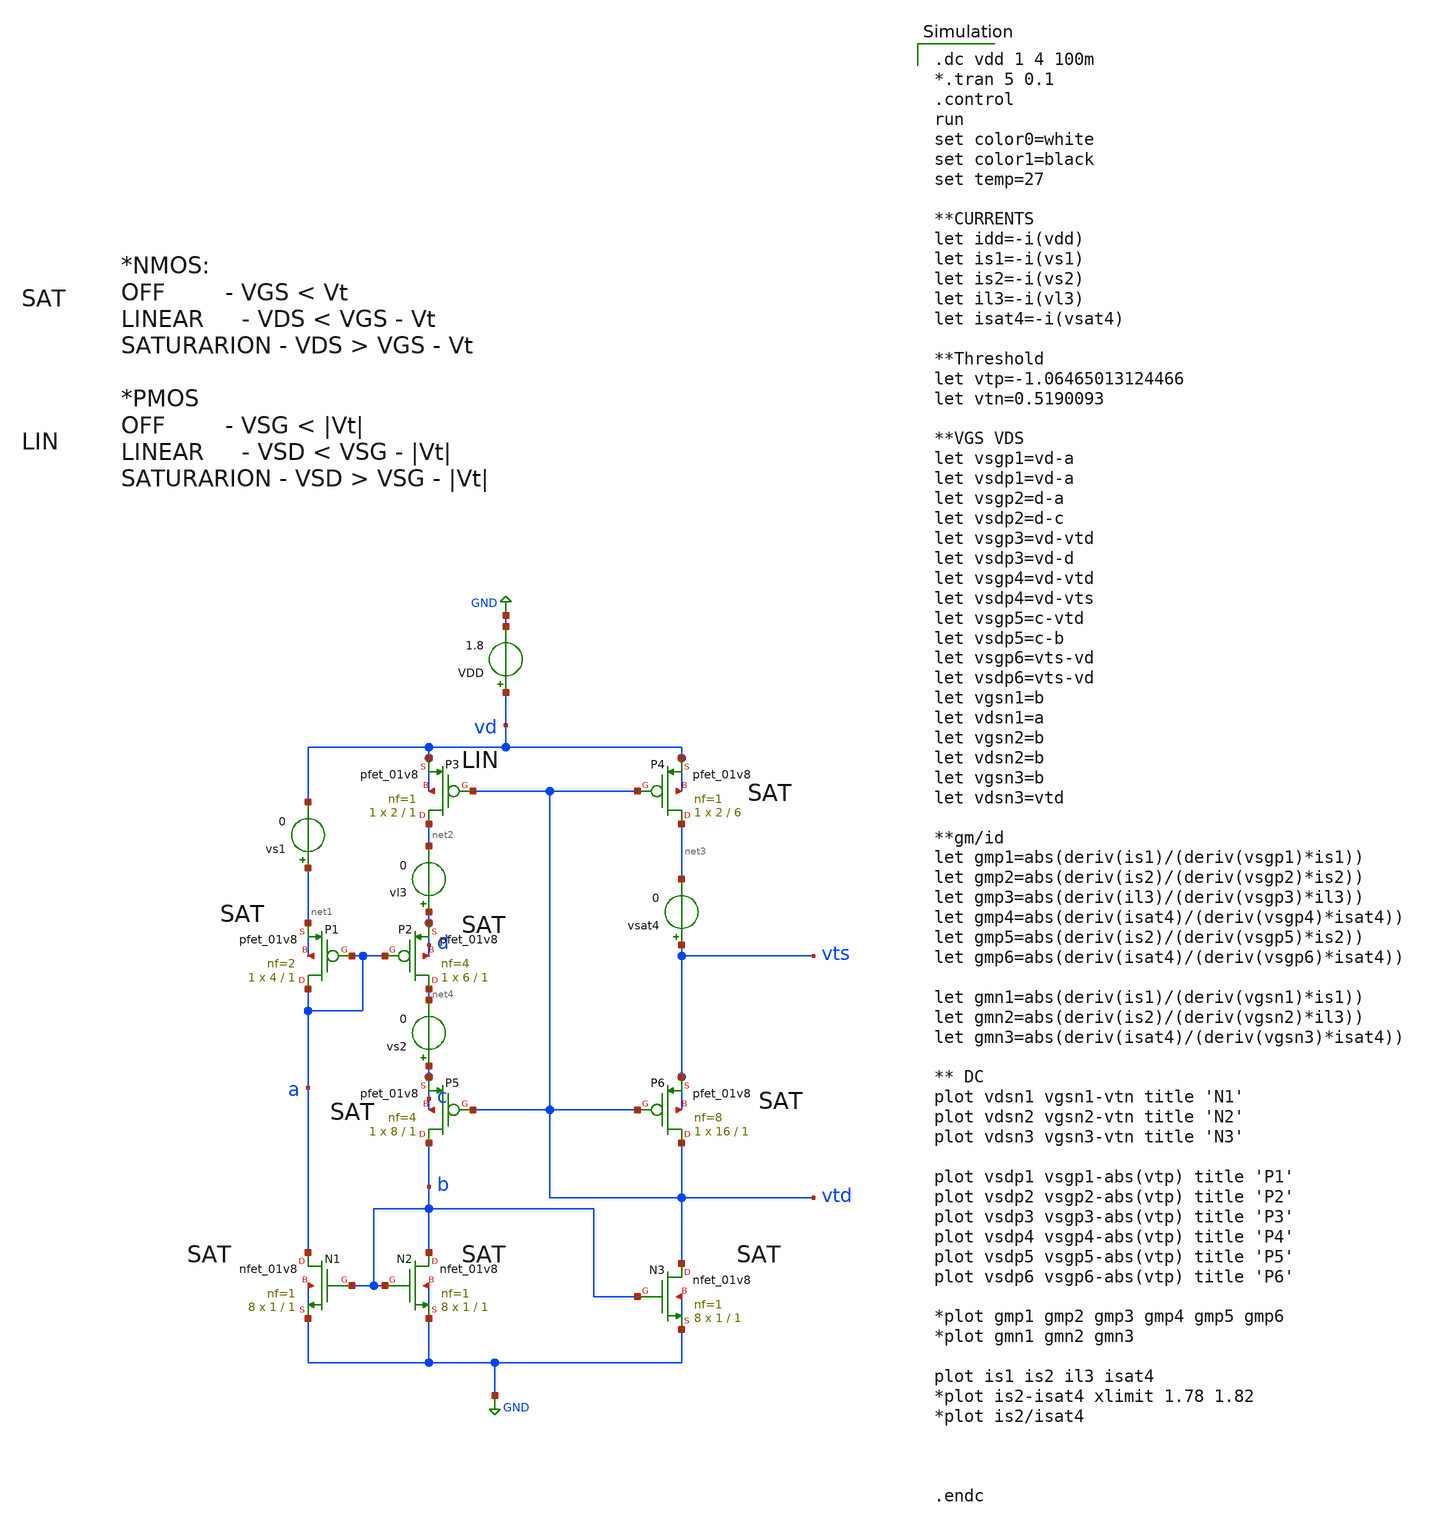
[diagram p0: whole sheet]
** sch_path: sensor/xschem/temp-tb-dc.sch
**.subckt temp-tb-dc
VDD vd GND 1.8
vs1 net1 vd 0
vs2 c net4 0
vl3 d net2 0
vsat4 vts net3 0
XP1 a a net1 net1 sky130_fd_pr__pfet_01v8 L=1 W=4 nf=2 ad='int((nf+1)/2) * W/nf * 0.29' as='int((nf+2)/2) * W/nf * 0.29'
+ pd='2*int((nf+1)/2) * (W/nf + 0.29)' ps='2*int((nf+2)/2) * (W/nf + 0.29)' nrd='0.29 / W' nrs='0.29 / W'
+ sa=0 sb=0 sd=0 mult=1 m=1
XP2 net4 a d d sky130_fd_pr__pfet_01v8 L=1 W=6 nf=4 ad='int((nf+1)/2) * W/nf * 0.29' as='int((nf+2)/2) * W/nf * 0.29'
+ pd='2*int((nf+1)/2) * (W/nf + 0.29)' ps='2*int((nf+2)/2) * (W/nf + 0.29)' nrd='0.29 / W' nrs='0.29 / W'
+ sa=0 sb=0 sd=0 mult=1 m=1
XP3 net2 vtd vd vd sky130_fd_pr__pfet_01v8 L=1 W=2 nf=1 ad='int((nf+1)/2) * W/nf * 0.29' as='int((nf+2)/2) * W/nf * 0.29'
+ pd='2*int((nf+1)/2) * (W/nf + 0.29)' ps='2*int((nf+2)/2) * (W/nf + 0.29)' nrd='0.29 / W' nrs='0.29 / W'
+ sa=0 sb=0 sd=0 mult=1 m=1
XP4 net3 vtd vd vd sky130_fd_pr__pfet_01v8 L=6 W=2 nf=1 ad='int((nf+1)/2) * W/nf * 0.29' as='int((nf+2)/2) * W/nf * 0.29'
+ pd='2*int((nf+1)/2) * (W/nf + 0.29)' ps='2*int((nf+2)/2) * (W/nf + 0.29)' nrd='0.29 / W' nrs='0.29 / W'
+ sa=0 sb=0 sd=0 mult=1 m=1
XP5 b vtd c c sky130_fd_pr__pfet_01v8 L=1 W=8 nf=4 ad='int((nf+1)/2) * W/nf * 0.29' as='int((nf+2)/2) * W/nf * 0.29'
+ pd='2*int((nf+1)/2) * (W/nf + 0.29)' ps='2*int((nf+2)/2) * (W/nf + 0.29)' nrd='0.29 / W' nrs='0.29 / W'
+ sa=0 sb=0 sd=0 mult=1 m=1
XP6 vtd vtd vts vts sky130_fd_pr__pfet_01v8 L=1 W=16 nf=8 ad='int((nf+1)/2) * W/nf * 0.29' as='int((nf+2)/2) * W/nf * 0.29'
+ pd='2*int((nf+1)/2) * (W/nf + 0.29)' ps='2*int((nf+2)/2) * (W/nf + 0.29)' nrd='0.29 / W' nrs='0.29 / W'
+ sa=0 sb=0 sd=0 mult=1 m=1
XN1 a b GND GND sky130_fd_pr__nfet_01v8 L=1 W=1 nf=1 ad='int((nf+1)/2) * W/nf * 0.29' as='int((nf+2)/2) * W/nf * 0.29'
+ pd='2*int((nf+1)/2) * (W/nf + 0.29)' ps='2*int((nf+2)/2) * (W/nf + 0.29)' nrd='0.29 / W' nrs='0.29 / W'
+ sa=0 sb=0 sd=0 mult=8 m=8
XN2 b b GND GND sky130_fd_pr__nfet_01v8 L=1 W=1 nf=1 ad='int((nf+1)/2) * W/nf * 0.29' as='int((nf+2)/2) * W/nf * 0.29'
+ pd='2*int((nf+1)/2) * (W/nf + 0.29)' ps='2*int((nf+2)/2) * (W/nf + 0.29)' nrd='0.29 / W' nrs='0.29 / W'
+ sa=0 sb=0 sd=0 mult=8 m=8
XN3 vtd b GND GND sky130_fd_pr__nfet_01v8 L=1 W=1 nf=1 ad='int((nf+1)/2) * W/nf * 0.29' as='int((nf+2)/2) * W/nf * 0.29'
+ pd='2*int((nf+1)/2) * (W/nf + 0.29)' ps='2*int((nf+2)/2) * (W/nf + 0.29)' nrd='0.29 / W' nrs='0.29 / W'
+ sa=0 sb=0 sd=0 mult=8 m=8
**** begin user architecture code

.dc vdd 1 4 100m
*.tran 5 0.1
.control
run
set color0=white
set color1=black
set temp=27

**CURRENTS
let idd=-i(vdd)
let is1=-i(vs1)
let is2=-i(vs2)
let il3=-i(vl3)
let isat4=-i(vsat4)

**Threshold
let vtp=-1.06465013124466
let vtn=0.5190093

**VGS VDS
let vsgp1=vd-a
let vsdp1=vd-a
let vsgp2=d-a
let vsdp2=d-c
let vsgp3=vd-vtd
let vsdp3=vd-d
let vsgp4=vd-vtd
let vsdp4=vd-vts
let vsgp5=c-vtd
let vsdp5=c-b
let vsgp6=vts-vd
let vsdp6=vts-vd
let vgsn1=b
let vdsn1=a
let vgsn2=b
let vdsn2=b
let vgsn3=b
let vdsn3=vtd

**gm/id
let gmp1=abs(deriv(is1)/(deriv(vsgp1)*is1))
let gmp2=abs(deriv(is2)/(deriv(vsgp2)*is2))
let gmp3=abs(deriv(il3)/(deriv(vsgp3)*il3))
let gmp4=abs(deriv(isat4)/(deriv(vsgp4)*isat4))
let gmp5=abs(deriv(is2)/(deriv(vsgp5)*is2))
let gmp6=abs(deriv(isat4)/(deriv(vsgp6)*isat4))

let gmn1=abs(deriv(is1)/(deriv(vgsn1)*is1))
let gmn2=abs(deriv(is2)/(deriv(vgsn2)*il3))
let gmn3=abs(deriv(isat4)/(deriv(vgsn3)*isat4))

** DC
plot vdsn1 vgsn1-vtn title 'N1'
plot vdsn2 vgsn2-vtn title 'N2'
plot vdsn3 vgsn3-vtn title 'N3'

plot vsdp1 vsgp1-abs(vtp) title 'P1'
plot vsdp2 vsgp2-abs(vtp) title 'P2'
plot vsdp3 vsgp3-abs(vtp) title 'P3'
plot vsdp4 vsgp4-abs(vtp) title 'P4'
plot vsdp5 vsgp5-abs(vtp) title 'P5'
plot vsdp6 vsgp6-abs(vtp) title 'P6'

*plot gmp1 gmp2 gmp3 gmp4 gmp5 gmp6
*plot gmn1 gmn2 gmn3

plot is1 is2 il3 isat4
*plot is2-isat4 xlimit 1.78 1.82
*plot is2/isat4



.endc



.lib /home/hugodg/sky130_workspace/skywater-pdk/libraries/sky130_fd_pr_ngspice/latest/models/sky130.lib.spice tt



R0 a.n2 a.t0 63.907
R1 a.n3 a.t2 63.628
R2 a.n0 a.t5 63.628
R3 a.n0 a.t4 63.628
R4 a.n0 a.t6 63.628
R5 a.n1 a.t3 14.282
R6 a.n1 a.t1 14.282
R7 a.n0 a.n3 2.215
R8 a a.n0 1.033
R9 a.n2 a.n1 0.526
R10 a.n3 a.n2 0.258
R11 vd.n6 vd.n5 411.106
R12 vd.n7 vd.n6 271.662
R13 vd.n15 vd.n10 271.436
R14 vd.n16 vd.n15 143.96
R15 vd.n8 vd.n7 6.519
R16 vd.n18 vd.n8 4
R17 vd vd.n18 3.145
R18 vd.n17 vd.n16 0.327
R19 vd.n18 vd.n17 0.174
R20 vd.n15 vd.n14 0.015
R21 vd.n12 vd.n11 0.008
R22 vd.n10 vd.n9 0.008
R23 vd.n5 vd.n4 0.008
R24 vd.n13 vd.n12 0.007
R25 vd.n6 vd.n3 0.006
R26 vd.n14 vd.n13 0.003
R27 vd.n1 vd.n0 0.003
R28 vd.n2 vd.n1 0.003
R29 vd.n3 vd.n2 0.002
R30 vtd.n15 vtd.t19 64.071
R31 vtd.n4 vtd.t4 63.721
R32 vtd.n17 vtd.t20 63.628
R33 vtd.n16 vtd.t17 63.628
R34 vtd.n15 vtd.t18 63.628
R35 vtd.n14 vtd.t6 63.628
R36 vtd.n12 vtd.t10 63.628
R37 vtd.n11 vtd.t8 63.628
R38 vtd.n9 vtd.t12 63.628
R39 vtd.n8 vtd.t14 63.628
R40 vtd.n6 vtd.t0 63.628
R41 vtd.n5 vtd.t2 63.628
R42 vtd.n19 vtd.t16 14.917
R43 vtd.n3 vtd.t5 14.282
R44 vtd.n3 vtd.t3 14.282
R45 vtd.n2 vtd.t1 14.282
R46 vtd.n2 vtd.t15 14.282
R47 vtd.n1 vtd.t13 14.282
R48 vtd.n1 vtd.t9 14.282
R49 vtd.n0 vtd.t11 14.282
R50 vtd.n0 vtd.t7 14.282
R51 vtd.n18 vtd.n17 1.082
R52 vtd.n16 vtd.n15 0.443
R53 vtd.n17 vtd.n16 0.443
R54 vtd vtd.n19 0.162
R55 vtd.n18 vtd.n14 0.128
R56 vtd.n19 vtd.n18 0.118
R57 vtd.n14 vtd.n13 0.096
R58 vtd.n6 vtd.n5 0.089
R59 vtd.n9 vtd.n8 0.089
R60 vtd.n12 vtd.n11 0.089
R61 vtd.n4 vtd.n3 0.063
R62 vtd.n7 vtd.n2 0.063
R63 vtd.n10 vtd.n1 0.063
R64 vtd.n13 vtd.n0 0.063
R65 vtd.n5 vtd.n4 0.044
R66 vtd.n7 vtd.n6 0.044
R67 vtd.n8 vtd.n7 0.044
R68 vtd.n10 vtd.n9 0.044
R69 vtd.n11 vtd.n10 0.044
R70 vtd.n13 vtd.n12 0.044
R71 b.n20 b.t16 38.817
R72 b.n4 b.t19 38.791
R73 b.n7 b.t22 38.779
R74 b.n10 b.t18 38.769
R75 b.n13 b.t23 38.759
R76 b.n15 b.t17 38.749
R77 b.n18 b.t21 38.741
R78 b.n19 b.t20 38.731
R79 b.n21 b.t24 38.471
R80 b.n5 b.t27 38.458
R81 b.n8 b.t30 38.452
R82 b.n11 b.t26 38.447
R83 b.n23 b.t28 38.193
R84 b.n3 b.t25 38.104
R85 b.n2 b.t31 38.064
R86 b.n26 b.t29 38.058
R87 b.n15 b.t12 37.359
R88 b.n13 b.t0 37.359
R89 b.n4 b.t8 37.359
R90 b.n7 b.t2 37.359
R91 b.n10 b.t10 37.359
R92 b.n18 b.t4 37.359
R93 b.n19 b.t6 37.359
R94 b.n20 b.t14 37.359
R95 b.n5 b.t9 17.617
R96 b.n24 b.t7 17.404
R97 b.n17 b.t5 17.404
R98 b.n14 b.t13 17.404
R99 b.n12 b.t1 17.404
R100 b.n9 b.t11 17.404
R101 b.n6 b.t3 17.404
R102 b.n22 b.t15 17.404
R103 b b.n26 1.727
R104 b.n3 b.n2 0.75
R105 b.n26 b.n3 0.708
R106 b.n6 b.n5 0.392
R107 b.n9 b.n8 0.388
R108 b.n14 b.n1 0.379
R109 b.n17 b.n16 0.375
R110 b.n25 b.n24 0.371
R111 b.n23 b.n22 0.367
R112 b.n0 b.n11 0.352
R113 b.n21 b.n20 0.345
R114 b.n5 b.n4 0.332
R115 b.n8 b.n7 0.326
R116 b.n11 b.n10 0.321
R117 b.n16 b.n15 0.311
R118 b.n25 b.n18 0.307
R119 b.n26 b.n25 0.291
R120 b.n23 b.n19 0.286
R121 b.n1 b.n13 0.254
R122 b.n25 b.n17 0.233
R123 b.n16 b.n14 0.229
R124 b.n11 b.n9 0.221
R125 b.n8 b.n6 0.217
R126 b.n1 b.n12 0.212
R127 b.n22 b.n21 0.2
R128 b.n24 b.n23 0.196
R129 b.n1 b.n0 0.124
R130 gnd.n10 gnd.n12 732.611
R131 gnd.n10 gnd.n14 732.611
R132 gnd.n1 gnd.n3 732.611
R133 gnd.n1 gnd.n5 732.611
R134 gnd.n0 gnd.n7 732.611
R135 gnd.n0 gnd.n9 732.611
R136 gnd.n15 gnd.n1 3.25
R137 gnd.n16 gnd.n10 3.137
R138 gnd.n15 gnd.n0 2.717
R139 gnd gnd.n16 0.192
R140 gnd.n16 gnd.n15 0.101
R141 gnd.n12 gnd.n11 0.004
R142 gnd.n14 gnd.n13 0.004
R143 gnd.n3 gnd.n2 0.004
R144 gnd.n5 gnd.n4 0.004
R145 gnd.n7 gnd.n6 0.004
R146 gnd.n9 gnd.n8 0.004
C0 vts c 0.22fF
C1 a c 0.61fF
C2 c d 0.88fF
C3 vts vtd 3.97fF
C4 b vts 1.25fF
C5 a vtd 0.62fF
C6 vtd d 0.24fF
C7 b a 1.24fF
C8 b d 0.04fF
C9 vts vd 0.45fF
C10 c vtd 1.16fF
C11 a vd 1.17fF
C12 d vd 0.94fF
C13 b c 0.61fF
C14 c vd 0.43fF
C15 b vtd 4.68fF
C16 vtd vd 0.78fF
C17 b vd 0.11fF
C18 a vts 0.37fF
C19 vts d 0.05fF
C20 a d 0.78fF
C21 b.n0 gnd 0.04fF $ **FLOATING
C22 b.n1 gnd 0.15fF $ **FLOATING
C23 b.t31 gnd 0.29fF
C24 b.n2 gnd 0.36fF $ **FLOATING
C25 b.t25 gnd 0.29fF
C26 b.n3 gnd 0.34fF $ **FLOATING
C27 b.t9 gnd 0.01fF
C28 b.t19 gnd 0.30fF
C29 b.t8 gnd 0.29fF
C30 b.n4 gnd 0.46fF $ **FLOATING
C31 b.t27 gnd 0.30fF
C32 b.n5 gnd 0.47fF $ **FLOATING
C33 b.t3 gnd 0.01fF
C34 b.n6 gnd 0.14fF $ **FLOATING
C35 b.t22 gnd 0.30fF
C36 b.t2 gnd 0.29fF
C37 b.n7 gnd 0.46fF $ **FLOATING
C38 b.t30 gnd 0.30fF
C39 b.n8 gnd 0.34fF $ **FLOATING
C40 b.t11 gnd 0.01fF
C41 b.n9 gnd 0.14fF $ **FLOATING
C42 b.t18 gnd 0.30fF
C43 b.t10 gnd 0.29fF
C44 b.n10 gnd 0.47fF $ **FLOATING
C45 b.t26 gnd 0.30fF
C46 b.n11 gnd 0.33fF $ **FLOATING
C47 b.t1 gnd 0.01fF
C48 b.n12 gnd 0.07fF $ **FLOATING
C49 b.t23 gnd 0.30fF
C50 b.t0 gnd 0.29fF
C51 b.n13 gnd 0.47fF $ **FLOATING
C52 b.t13 gnd 0.01fF
C53 b.n14 gnd 0.14fF $ **FLOATING
C54 b.t17 gnd 0.30fF
C55 b.t12 gnd 0.29fF
C56 b.n15 gnd 0.47fF $ **FLOATING
C57 b.n16 gnd 0.09fF $ **FLOATING
C58 b.t5 gnd 0.01fF
C59 b.n17 gnd 0.14fF $ **FLOATING
C60 b.t21 gnd 0.30fF
C61 b.t4 gnd 0.29fF
C62 b.n18 gnd 0.48fF $ **FLOATING
C63 b.t7 gnd 0.01fF
C64 b.t20 gnd 0.30fF
C65 b.t6 gnd 0.29fF
C66 b.n19 gnd 0.48fF $ **FLOATING
C67 b.t28 gnd 0.29fF
C68 b.t16 gnd 0.30fF
C69 b.t14 gnd 0.29fF
C70 b.n20 gnd 0.46fF $ **FLOATING
C71 b.t24 gnd 0.30fF
C72 b.n21 gnd 0.32fF $ **FLOATING
C73 b.t15 gnd 0.01fF
C74 b.n22 gnd 0.13fF $ **FLOATING
C75 b.n23 gnd 0.39fF $ **FLOATING
C76 b.n24 gnd 0.13fF $ **FLOATING
C77 b.n25 gnd 0.09fF $ **FLOATING
C78 b.t29 gnd 0.29fF
C79 b.n26 gnd 0.48fF $ **FLOATING
C80 vtd.t16 gnd 4.79fF
C81 vtd.t11 gnd 0.04fF
C82 vtd.t7 gnd 0.04fF
C83 vtd.n0 gnd 0.19fF $ **FLOATING
C84 vtd.t13 gnd 0.04fF
C85 vtd.t9 gnd 0.04fF
C86 vtd.n1 gnd 0.19fF $ **FLOATING
C87 vtd.t1 gnd 0.04fF
C88 vtd.t15 gnd 0.04fF
C89 vtd.n2 gnd 0.19fF $ **FLOATING
C90 vtd.t5 gnd 0.04fF
C91 vtd.t3 gnd 0.04fF
C92 vtd.n3 gnd 0.19fF $ **FLOATING
C93 vtd.t4 gnd 0.68fF
C94 vtd.n4 gnd 4.85fF $ **FLOATING
C95 vtd.t2 gnd 0.67fF
C96 vtd.n5 gnd 0.73fF $ **FLOATING
C97 vtd.t0 gnd 0.67fF
C98 vtd.n6 gnd 0.73fF $ **FLOATING
C99 vtd.n7 gnd 0.32fF $ **FLOATING
C100 vtd.t14 gnd 0.67fF
C101 vtd.n8 gnd 0.73fF $ **FLOATING
C102 vtd.t12 gnd 0.67fF
C103 vtd.n9 gnd 0.73fF $ **FLOATING
C104 vtd.n10 gnd 0.32fF $ **FLOATING
C105 vtd.t8 gnd 0.67fF
C106 vtd.n11 gnd 0.73fF $ **FLOATING
C107 vtd.t10 gnd 0.67fF
C108 vtd.n12 gnd 0.73fF $ **FLOATING
C109 vtd.n13 gnd 0.28fF $ **FLOATING
C110 vtd.t6 gnd 0.67fF
C111 vtd.n14 gnd 0.38fF $ **FLOATING
C112 vtd.t20 gnd 0.67fF
C113 vtd.t17 gnd 0.67fF
C114 vtd.t18 gnd 0.67fF
C115 vtd.t19 gnd 0.68fF
C116 vtd.n15 gnd 0.76fF $ **FLOATING
C117 vtd.n16 gnd 0.39fF $ **FLOATING
C118 vtd.n17 gnd 0.45fF $ **FLOATING
C119 vtd.n18 gnd 0.38fF $ **FLOATING
C120 vtd.n19 gnd 3.72fF $ **FLOATING
C121 vd.n0 gnd 0.22fF $ **FLOATING
C122 vd.n1 gnd 0.26fF $ **FLOATING
C123 vd.n2 gnd 2.16fF $ **FLOATING
C124 vd.n3 gnd 2.29fF $ **FLOATING
C125 vd.n4 gnd 2.73fF $ **FLOATING
C126 vd.n5 gnd 0.26fF $ **FLOATING
C127 vd.n6 gnd 0.34fF $ **FLOATING
C128 vd.n7 gnd 3.51fF $ **FLOATING
C129 vd.n8 gnd 3.31fF $ **FLOATING
C130 vd.n9 gnd 1.56fF $ **FLOATING
C131 vd.n10 gnd 0.17fF $ **FLOATING
C132 vd.n11 gnd 0.13fF $ **FLOATING
C133 vd.n12 gnd 0.17fF $ **FLOATING
C134 vd.n13 gnd 1.08fF $ **FLOATING
C135 vd.n14 gnd 1.17fF $ **FLOATING
C136 vd.n15 gnd 0.22fF $ **FLOATING
C137 vd.n16 gnd 1.86fF $ **FLOATING
C138 vd.n17 gnd 1.03fF $ **FLOATING
C139 vd.n18 gnd 3.42fF $ **FLOATING
C140 a.n0 gnd 1.30fF $ **FLOATING
C141 a.t6 gnd 0.34fF
C142 a.t4 gnd 0.34fF
C143 a.t5 gnd 0.34fF
C144 a.t2 gnd 0.34fF
C145 a.t0 gnd 0.34fF
C146 a.t3 gnd 0.02fF
C147 a.t1 gnd 0.02fF
C148 a.n1 gnd 0.12fF $ **FLOATING
C149 a.n2 gnd 0.22fF $ **FLOATING
C150 a.n3 gnd 0.26fF $ **FLOATING
C151 b gnd 13.18fF
C152 c gnd 3.78fF
C153 vts gnd 19.40fF
C154 d gnd 4.70fF
C155 vtd gnd 8.09fF
C156 vd gnd 20.66fF
C157 a gnd -2.91fF


**** end user architecture code
**.ends
.GLOBAL GND
.end
